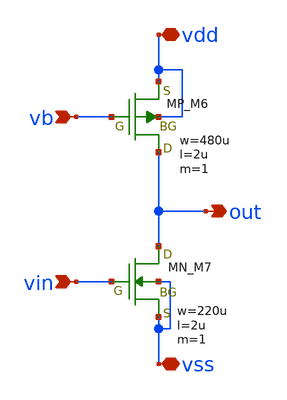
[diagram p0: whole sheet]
** sch_path: member_project/opamp/makoto645/testbench/cs.sch
**.subckt cs vb vin out vss vdd
*.ipin vb
*.ipin vin
*.opin out
*.iopin vss
*.iopin vdd
XM6 out vb vdd vdd PMOS w=480u l=2u as=0 ad=0 ps=0 pd=0 nrd=0 nrs=0 m=1
XM7 out vin vss vss NMOS w=220u l=2u as=0 ad=0 ps=0 pd=0 nrd=0 nrs=0 m=1
**.ends
.end
